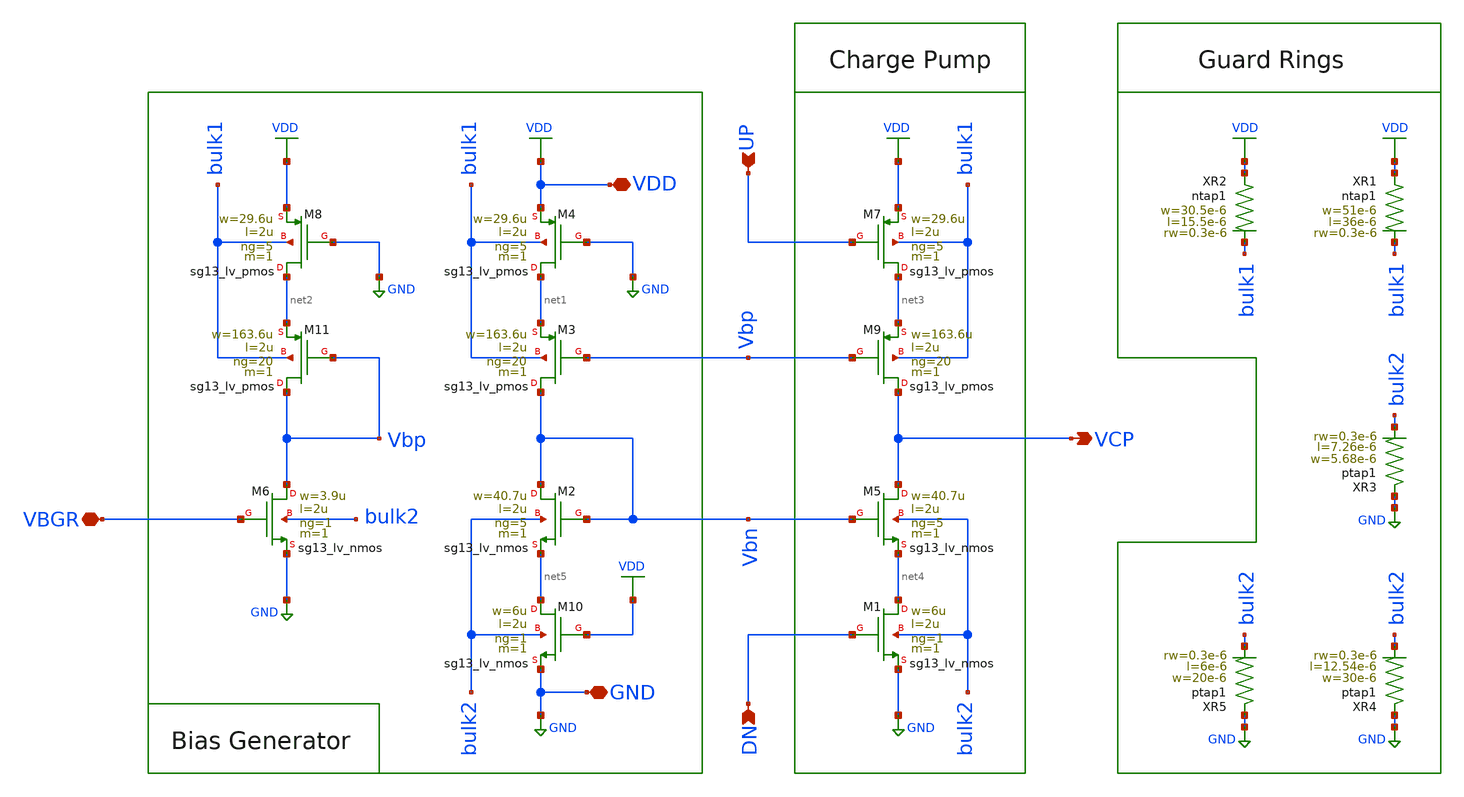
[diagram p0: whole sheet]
** sch_path: xschem/CHARGE_PUMP.sch
**.subckt CHARGE_PUMP VCP UP DN GND VBGR VDD
*.opin VCP
*.ipin UP
*.ipin DN
*.iopin GND
*.iopin VBGR
*.iopin VDD
XM2 Vbn Vbn net5 bulk2 sg13_lv_nmos w=40.7u l=2u ng=5 m=1 mm_ok=1
XM8 net2 GND VDD bulk1 sg13_lv_pmos w=29.6u l=2u ng=5 m=1 mm_ok=1
XM11 Vbp Vbp net2 bulk1 sg13_lv_pmos w=163.6u l=2u ng=20 m=1 mm_ok=1
XM3 Vbn Vbp net1 bulk1 sg13_lv_pmos w=163.6u l=2u ng=20 m=1 mm_ok=1
XM4 net1 GND VDD bulk1 sg13_lv_pmos w=29.6u l=2u ng=5 m=1 mm_ok=1
XM7 net3 UP VDD bulk1 sg13_lv_pmos w=29.6u l=2u ng=5 m=1 mm_ok=1
XM9 VCP Vbp net3 bulk1 sg13_lv_pmos w=163.6u l=2u ng=20 m=1 mm_ok=1
XM10 net5 VDD GND bulk2 sg13_lv_nmos w=6u l=2u ng=1 m=1 mm_ok=1
XM1 net4 DN GND bulk2 sg13_lv_nmos w=6u l=2u ng=1 m=1 mm_ok=1
XM5 VCP Vbn net4 bulk2 sg13_lv_nmos w=40.7u l=2u ng=5 m=1 mm_ok=1
XM6 Vbp VBGR GND bulk2 sg13_lv_nmos w=3.9u l=2u ng=1 m=1 mm_ok=1
XR1 VDD bulk1 ntap1 R=1.319 w=51e-6 l=36e-6 rw=0.3e-6
XR2 VDD bulk1 ntap1 R=2.51 w=30.5e-6 l=15.5e-6 rw=0.3e-6
XR3 GND bulk2 ptap1 R=9.234 w=5.68e-6 l=7.26e-6 rw=0.3e-6
XR4 GND bulk2 ptap1 R=2.717 w=30e-6 l=12.54e-6 rw=0.3e-6
XR5 GND bulk2 ptap1 R=4.486 w=20e-6 l=6e-6 rw=0.3e-6
**.ends
.GLOBAL GND
.GLOBAL VDD
.end
